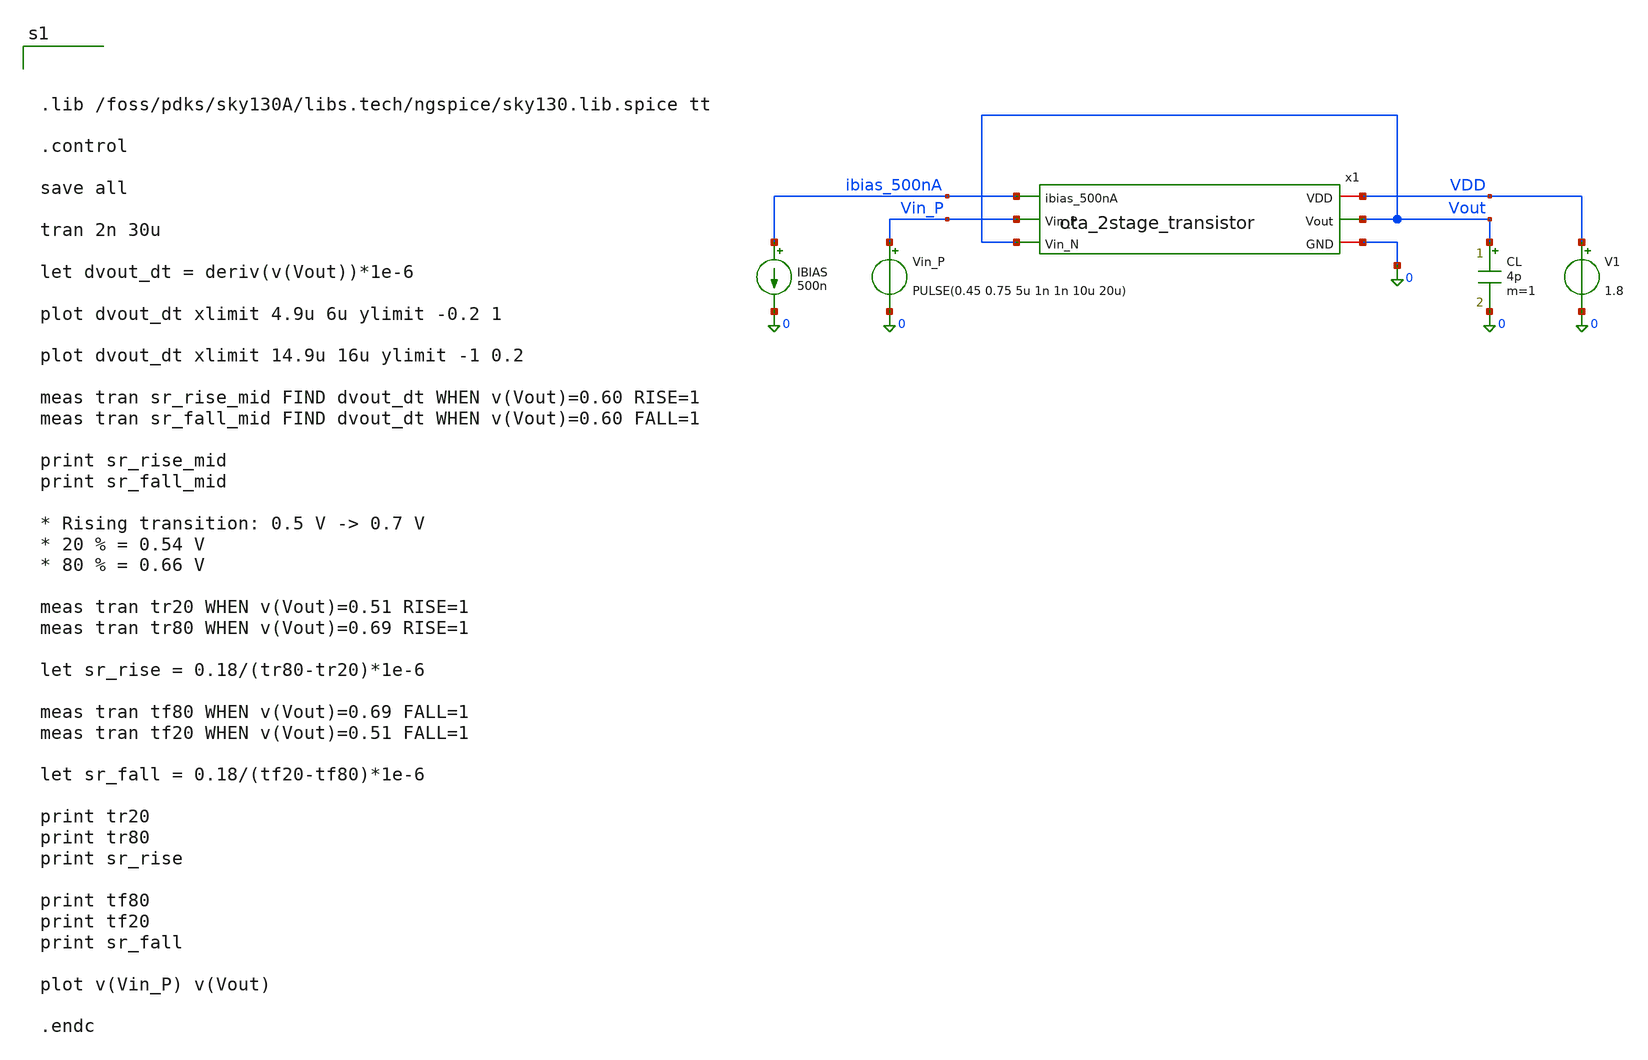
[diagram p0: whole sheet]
** sch_path: dfii/project_2stage_OTA_sim/tb_ota_2stage_slew.sch
**.subckt tb_ota_2stage_slew
x1 VDD ibias_500nA Vout Vin_P Vout 0 ota_2stage_transistor
V1 VDD 0 1.8
IBIAS ibias_500nA 0 500n
Vin_P Vin_P 0 PULSE(0.45 0.75 5u 1n 1n 10u 20u)
CL Vout 0 4p m=1
**** begin user architecture code



.lib /foss/pdks/sky130A/libs.tech/ngspice/sky130.lib.spice tt

.control

save all

tran 2n 30u

let dvout_dt = deriv(v(Vout))*1e-6

plot dvout_dt xlimit 4.9u 6u ylimit -0.2 1

plot dvout_dt xlimit 14.9u 16u ylimit -1 0.2

meas tran sr_rise_mid FIND dvout_dt WHEN v(Vout)=0.60 RISE=1
meas tran sr_fall_mid FIND dvout_dt WHEN v(Vout)=0.60 FALL=1

print sr_rise_mid
print sr_fall_mid

* Rising transition: 0.5 V -> 0.7 V
* 20 % = 0.54 V
* 80 % = 0.66 V

meas tran tr20 WHEN v(Vout)=0.51 RISE=1
meas tran tr80 WHEN v(Vout)=0.69 RISE=1

let sr_rise = 0.18/(tr80-tr20)*1e-6

meas tran tf80 WHEN v(Vout)=0.69 FALL=1
meas tran tf20 WHEN v(Vout)=0.51 FALL=1

let sr_fall = 0.18/(tf20-tf80)*1e-6

print tr20
print tr80
print sr_rise

print tf80
print tf20
print sr_fall

plot v(Vin_P) v(Vout)

.endc



**** end user architecture code
**.ends

* expanding   symbol:
*+  /foss/designs/project_2stage_OTA/dfii/project_2stage_OTA/ota_2stage_transistor.sym # of pins=6
** sym_path: dfii/project_2stage_OTA/ota_2stage_transistor.sym
** sch_path: dfii/project_2stage_OTA/ota_2stage_transistor.sch
.subckt ota_2stage_transistor VDD ibias_500nA Vout Vin_P Vin_N GND
*.iopin VDD
*.iopin GND
*.ipin ibias_500nA
*.ipin Vin_N
*.ipin Vin_P
*.opin Vout
XNLOAD_0 vdiode_n vdiode_n GND GND sky130_fd_pr__nfet_01v8 L=12 W=3.6 nf=1 ad='int((1 + 1)/2) * 3.6 / 1 * 0.29'
+ as='int((1 + 2)/2) * 3.6 / 1 * 0.29' pd='2*int((1 + 1)/2) * (3.6 / 1 + 0.29)' ps='2*int((1 + 2)/2) * (3.6 / 1 + 0.29)'
+ nrd='0.29 / 3.6 ' nrs='0.29 / 3.6 ' sa=0 sb=0 sd=0 mult=1 m=1
XNLOAD_1 out_s1 vdiode_n GND GND sky130_fd_pr__nfet_01v8 L=12 W=3.6 nf=1 ad='int((1 + 1)/2) * 3.6 / 1 * 0.29'
+ as='int((1 + 2)/2) * 3.6 / 1 * 0.29' pd='2*int((1 + 1)/2) * (3.6 / 1 + 0.29)' ps='2*int((1 + 2)/2) * (3.6 / 1 + 0.29)'
+ nrd='0.29 / 3.6 ' nrs='0.29 / 3.6 ' sa=0 sb=0 sd=0 mult=1 m=1
XNLOAD_2 Vout out_s1 GND GND sky130_fd_pr__nfet_01v8 L=2 W=3.6 nf=1 ad='int((1 + 1)/2) * 3.6 / 1 * 0.29'
+ as='int((1 + 2)/2) * 3.6 / 1 * 0.29' pd='2*int((1 + 1)/2) * (3.6 / 1 + 0.29)' ps='2*int((1 + 2)/2) * (3.6 / 1 + 0.29)'
+ nrd='0.29 / 3.6 ' nrs='0.29 / 3.6 ' sa=0 sb=0 sd=0 mult=2 m=2
XPDIFF_N vdiode_n Vin_N VCM VCM sky130_fd_pr__pfet_01v8 L=1 W=7.4 nf=1 ad='int((1 + 1)/2) * 7.4 / 1 * 0.29'
+ as='int((1 + 2)/2) * 7.4 / 1 * 0.29' pd='2*int((1 + 1)/2) * (7.4 / 1 + 0.29)' ps='2*int((1 + 2)/2) * (7.4 / 1 + 0.29)'
+ nrd='0.29 / 7.4 ' nrs='0.29 / 7.4 ' sa=0 sb=0 sd=0 mult=12 m=12
XPDIFF_P out_s1 Vin_P VCM VCM sky130_fd_pr__pfet_01v8 L=1 W=7.4 nf=1 ad='int((1 + 1)/2) * 7.4 / 1 * 0.29'
+ as='int((1 + 2)/2) * 7.4 / 1 * 0.29' pd='2*int((1 + 1)/2) * (7.4 / 1 + 0.29)' ps='2*int((1 + 2)/2) * (7.4 / 1 + 0.29)'
+ nrd='0.29 / 7.4 ' nrs='0.29 / 7.4 ' sa=0 sb=0 sd=0 mult=12 m=12
XPTAIL_1 VCM ibias_500nA VDD VDD sky130_fd_pr__pfet_01v8 L=1 W=1.76 nf=1 ad='int((1 + 1)/2) * 1.76 / 1 * 0.29'
+ as='int((1 + 2)/2) * 1.76 / 1 * 0.29' pd='2*int((1 + 1)/2) * (1.76 / 1 + 0.29)' ps='2*int((1 + 2)/2) * (1.76 / 1 + 0.29)'
+ nrd='0.29 / 1.76 ' nrs='0.29 / 1.76 ' sa=0 sb=0 sd=0 mult=1 m=1
XPTAIL_2 Vout ibias_500nA VDD VDD sky130_fd_pr__pfet_01v8 L=1 W=1.76 nf=1 ad='int((1 + 1)/2) * 1.76 / 1 * 0.29'
+ as='int((1 + 2)/2) * 1.76 / 1 * 0.29' pd='2*int((1 + 1)/2) * (1.76 / 1 + 0.29)' ps='2*int((1 + 2)/2) * (1.76 / 1 + 0.29)'
+ nrd='0.29 / 1.76 ' nrs='0.29 / 1.76 ' sa=0 sb=0 sd=0 mult=6 m=6
XPTAIL_0 ibias_500nA ibias_500nA VDD VDD sky130_fd_pr__pfet_01v8 L=1 W=1.76 nf=1 ad='int((1 + 1)/2) * 1.76 / 1 * 0.29'
+ as='int((1 + 2)/2) * 1.76 / 1 * 0.29' pd='2*int((1 + 1)/2) * (1.76 / 1 + 0.29)' ps='2*int((1 + 2)/2) * (1.76 / 1 + 0.29)'
+ nrd='0.29 / 1.76 ' nrs='0.29 / 1.76 ' sa=0 sb=0 sd=0 mult=1 m=1
XCMILLER out_s1 net1 sky130_fd_pr__cap_mim_m3_1 W=19 L=19 MF=1 m=1
XRMILLER Vout net1 GND sky130_fd_pr__res_xhigh_po_0p35 L=31.5 mult=1 m=1
.ends

.GLOBAL VDD
.end
